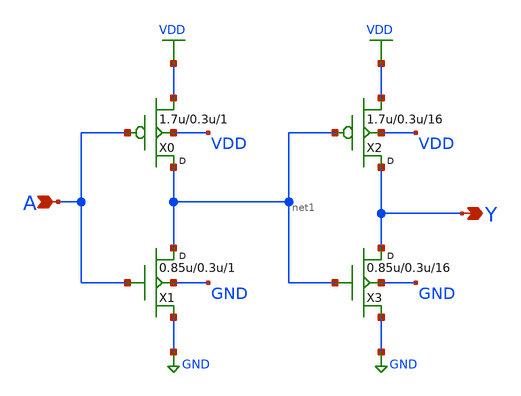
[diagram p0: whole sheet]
** sch_path: lib/12T/buf16/gf180mcu_osu_sc_buf_16.sch
**.subckt gf180mcu_osu_sc_buf_16 A Y
*.ipin A
*.opin Y
X0 net1 A VDD VDD pmos_3p3 w=1.7u l=0.3u m=1
X1 net1 A GND GND nmos_3p3 w=0.85u l=0.3u m=1
X2 Y net1 VDD VDD pmos_3p3 w=1.7u l=0.3u m=16
X3 Y net1 GND GND nmos_3p3 w=0.85u l=0.3u m=16
**.ends
.GLOBAL VDD
.GLOBAL GND
.end
